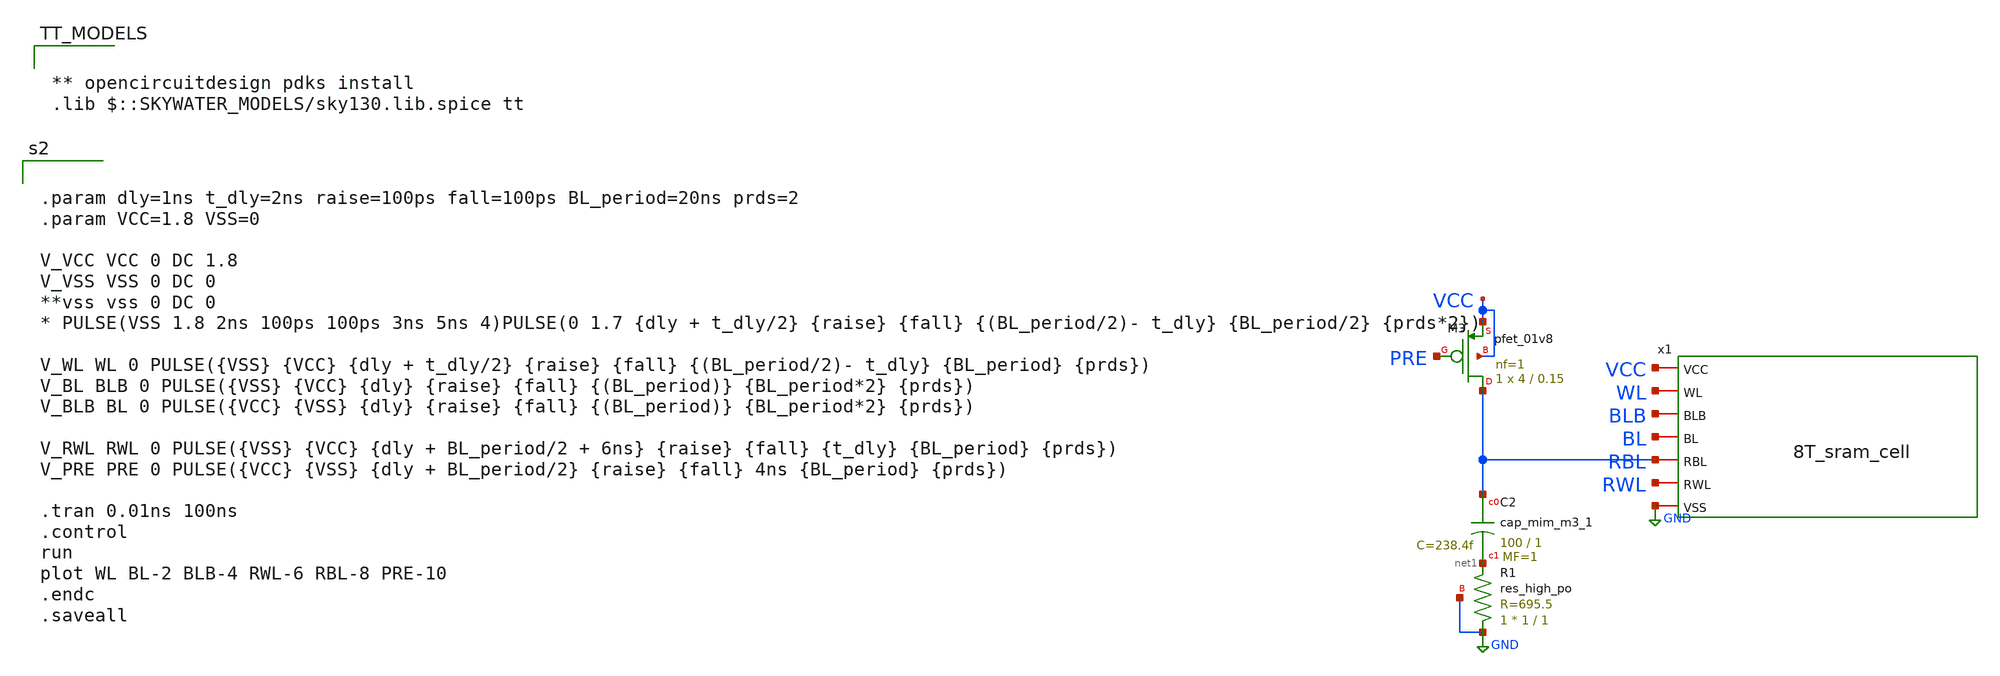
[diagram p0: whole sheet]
** sch_path: work.sch
**.subckt work
x1 VCC WL BLB BL RBL RWL GND 8T_sram_cell
XC2 RBL net1 sky130_fd_pr__cap_mim_m3_1 W=100 L=1 MF=1 m=1
XM3 RBL PRE VCC VCC sky130_fd_pr__pfet_01v8 L=0.15 W=4 nf=1 ad='int((1 + 1)/2) * 4 / 1 * 0.29' as='int((1 + 2)/2) * 4 / 1 * 0.29'
+ pd='2*int((1 + 1)/2) * (4 / 1 + 0.29)' ps='2*int((1 + 2)/2) * (4 / 1 + 0.29)' nrd='0.29 / 4 ' nrs='0.29 / 4 '
+ sa=0 sb=0 sd=0 mult=1 m=1
XR1 GND net1 GND sky130_fd_pr__res_high_po W=1 L=1 mult=1 m=1
**** begin user architecture code


.param dly=1ns t_dly=2ns raise=100ps fall=100ps BL_period=20ns prds=2
.param VCC=1.8 VSS=0

V_VCC VCC 0 DC 1.8
V_VSS VSS 0 DC 0
**vss vss 0 DC 0
* PULSE(VSS 1.8 2ns 100ps 100ps 3ns 5ns 4)PULSE(0 1.7 {dly + t_dly/2} {raise} {fall} {(BL_period/2)- t_dly}
*+ {BL_period/2} {prds*2})

V_WL WL 0 PULSE({VSS} {VCC} {dly + t_dly/2} {raise} {fall} {(BL_period/2)- t_dly} {BL_period} {prds})
V_BL BLB 0 PULSE({VSS} {VCC} {dly} {raise} {fall} {(BL_period)} {BL_period*2} {prds})
V_BLB BL 0 PULSE({VCC} {VSS} {dly} {raise} {fall} {(BL_period)} {BL_period*2} {prds})

V_RWL RWL 0 PULSE({VSS} {VCC} {dly + BL_period/2 + 6ns} {raise} {fall} {t_dly} {BL_period} {prds})
V_PRE PRE 0 PULSE({VCC} {VSS} {dly + BL_period/2} {raise} {fall} 4ns {BL_period} {prds})

.tran 0.01ns 100ns
.control
run
plot WL BL-2 BLB-4 RWL-6 RBL-8 PRE-10
.endc
.saveall




** opencircuitdesign pdks install
.lib $::SKYWATER_MODELS/sky130.lib.spice tt

**** end user architecture code
**.ends

* expanding   symbol:  8T_sram_cell.sym # of pins=7
** sym_path: 8T_sram_cell.sym
** sch_path: 8T_sram_cell.sch
.subckt 8T_sram_cell VCC WL BLB BL RBL RWL VSS
*.iopin VCC
*.iopin BLB
*.iopin WL
*.iopin BL
*.iopin VSS
*.iopin RBL
*.iopin RWL
XM1 q_bar q VSS VSS sky130_fd_pr__nfet_01v8 L=0.15 W=1 nf=1 ad='int((1 + 1)/2) * 1 / 1 * 0.29' as='int((1 + 2)/2) * 1 / 1 * 0.29'
+ pd='2*int((1 + 1)/2) * (1 / 1 + 0.29)' ps='2*int((1 + 2)/2) * (1 / 1 + 0.29)' nrd='0.29 / 1 ' nrs='0.29 / 1 '
+ sa=0 sb=0 sd=0 mult=1 m=1
XM2 q q_bar VSS VSS sky130_fd_pr__nfet_01v8 L=0.15 W=1 nf=1 ad='int((1 + 1)/2) * 1 / 1 * 0.29' as='int((1 + 2)/2) * 1 / 1 * 0.29'
+ pd='2*int((1 + 1)/2) * (1 / 1 + 0.29)' ps='2*int((1 + 2)/2) * (1 / 1 + 0.29)' nrd='0.29 / 1 ' nrs='0.29 / 1 '
+ sa=0 sb=0 sd=0 mult=1 m=1
XM3 q_bar q VCC VCC sky130_fd_pr__pfet_01v8 L=0.15 W=4 nf=1 ad='int((1 + 1)/2) * 4 / 1 * 0.29' as='int((1 + 2)/2) * 4 / 1 * 0.29'
+ pd='2*int((1 + 1)/2) * (4 / 1 + 0.29)' ps='2*int((1 + 2)/2) * (4 / 1 + 0.29)' nrd='0.29 / 4 ' nrs='0.29 / 4 '
+ sa=0 sb=0 sd=0 mult=1 m=1
XM4 q q_bar VCC VCC sky130_fd_pr__pfet_01v8 L=0.15 W=4 nf=1 ad='int((1 + 1)/2) * 4 / 1 * 0.29' as='int((1 + 2)/2) * 4 / 1 * 0.29'
+ pd='2*int((1 + 1)/2) * (4 / 1 + 0.29)' ps='2*int((1 + 2)/2) * (4 / 1 + 0.29)' nrd='0.29 / 4 ' nrs='0.29 / 4 '
+ sa=0 sb=0 sd=0 mult=1 m=1
XM5 BLB WL q_bar VSS sky130_fd_pr__nfet_01v8 L=0.15 W=1 nf=1 ad='int((1 + 1)/2) * 1 / 1 * 0.29' as='int((1 + 2)/2) * 1 / 1 * 0.29'
+ pd='2*int((1 + 1)/2) * (1 / 1 + 0.29)' ps='2*int((1 + 2)/2) * (1 / 1 + 0.29)' nrd='0.29 / 1 ' nrs='0.29 / 1 '
+ sa=0 sb=0 sd=0 mult=1 m=1
XM8 q WL BL VSS sky130_fd_pr__nfet_01v8 L=0.15 W=1 nf=1 ad='int((1 + 1)/2) * 1 / 1 * 0.29' as='int((1 + 2)/2) * 1 / 1 * 0.29'
+ pd='2*int((1 + 1)/2) * (1 / 1 + 0.29)' ps='2*int((1 + 2)/2) * (1 / 1 + 0.29)' nrd='0.29 / 1 ' nrs='0.29 / 1 '
+ sa=0 sb=0 sd=0 mult=1 m=1
XM6 net1 q_bar VSS VSS sky130_fd_pr__nfet_01v8 L=0.15 W=1 nf=1 ad='int((1 + 1)/2) * 1 / 1 * 0.29' as='int((1 + 2)/2) * 1 / 1 * 0.29'
+ pd='2*int((1 + 1)/2) * (1 / 1 + 0.29)' ps='2*int((1 + 2)/2) * (1 / 1 + 0.29)' nrd='0.29 / 1 ' nrs='0.29 / 1 '
+ sa=0 sb=0 sd=0 mult=1 m=1
XM7 RBL RWL net1 VSS sky130_fd_pr__nfet_01v8 L=0.15 W=1 nf=1 ad='int((1 + 1)/2) * 1 / 1 * 0.29' as='int((1 + 2)/2) * 1 / 1 * 0.29'
+ pd='2*int((1 + 1)/2) * (1 / 1 + 0.29)' ps='2*int((1 + 2)/2) * (1 / 1 + 0.29)' nrd='0.29 / 1 ' nrs='0.29 / 1 '
+ sa=0 sb=0 sd=0 mult=1 m=1
.ends

.GLOBAL GND
.end
